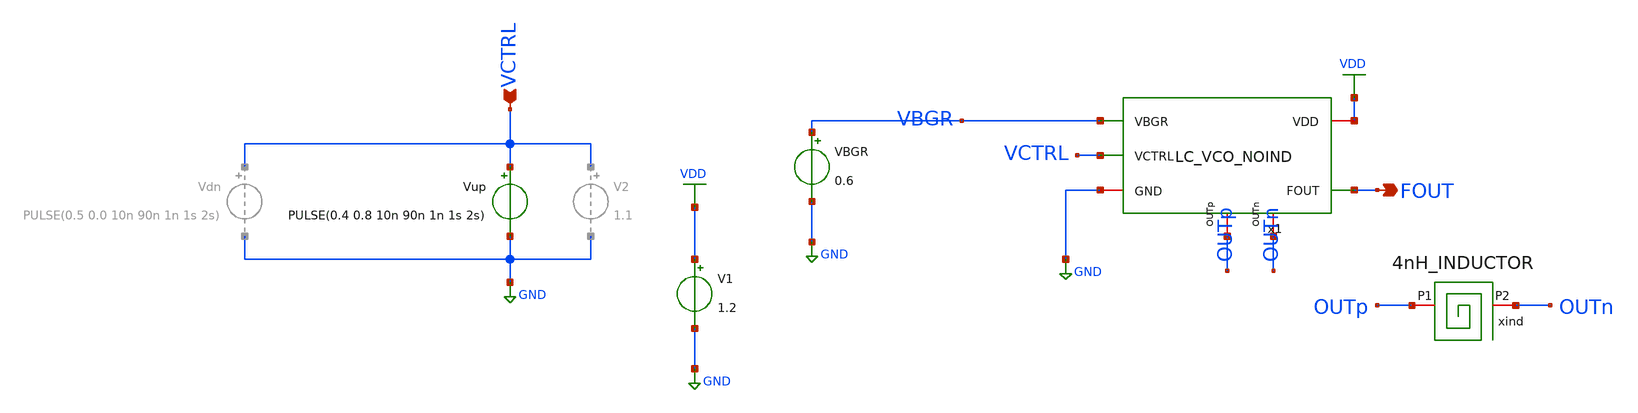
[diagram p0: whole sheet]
** sch_path: xschem/lc-vco/LC_VCO_PEX_tb.sch
**.subckt LC_VCO_PEX_tb FOUT VCTRL
*.opin FOUT
*.ipin VCTRL
VBGR VBGR GND 0.6
x1 OUTp OUTn FOUT VCTRL VBGR GND VDD LC_VCO_NOIND
V1 VDD GND 1.2
xind OUTp OUTn 4nH_INDUCTOR
Vup VCTRL GND PULSE(0.4 0.8 10n 90n 1n 1s 2s)
**** begin user architecture code



.param temp = 27
.options method=gear rshunt=1.0e12
* start-up kick: a noise-free run can stay at the unstable equilibrium
.ic v(OUTp)=0.4

.control

* Save required signals
save v(VCTRL) v(FOUT) v(OUTn) v(OUTp)

* Long transient simulation
tran 10p 500n 100n

* Save raw waveform
write tb_LC_VCO_PEX_tran.raw

* Plot transient waveform
let vout = v(FOUT)
plot v(VCTRL) v(OUTn) v(FOUT) v(OUTp)

* Plot steady-state waveform
plot v(VCTRL) v(OUTn) v(FOUT) v(OUTp) xlimit 400n 405n

* FFT analysis
setplot tran1
linearize vout
set specwindow=blackman
fft vout

* Plot FFT spectrum
let power_out_db = db(vout)
plot power_out_db xlimit 2.34G 2.54G ylimit -200 0

* Find the maximum magnitude value between 2G and 3G
meas sp max_power_out_db max power_out_db FROM=2G TO=3G

* Save FFT spectrum as raw file
write LC_VCO_PEX_fft.raw frequency power_out_db
shell python3 ../xschem/lc-vco/raw_spectrum_as_tran.py LC_VCO_PEX_fft.raw

* Save FFT data
wrdata fft_output_pex.txt frequency power_out_db

* Save waveform for external processing
wrdata vco_waveform_pex.txt power_out_db

.endc






.param temp=27
.control
save all
op
write LC_VCO_PEX_tb.raw
.endc




.include 4nH_INDUCTOR.spice
* Magic RC extraction of the VCO without its inductor (the inductor is the EM model above)
.include ../pex/LC_VCO_NOIND__LC_VCO_NOIND/magic_RC/LC_VCO_NOIND.pex_sim.spice


.lib cornerMOSlv.lib mos_tt
.lib cornerMOShv.lib mos_tt
.lib cornerRES.lib res_typ
.lib cornerCAP.lib cap_typ

**** end user architecture code
**.ends
.GLOBAL GND
.GLOBAL VDD
.end
